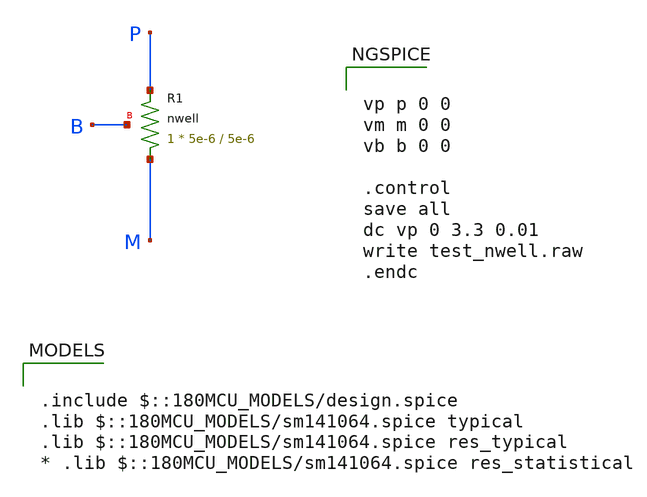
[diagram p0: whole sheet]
** sch_path: cells/xschem/tests/test_nwell.sch
* Copyright 2022 GlobalFoundries PDK Authors
* Licensed under the Apache License, Version 2.0 (the "License");
* you may not use this file except in compliance with the License.
* You may obtain a copy of the License at
* https://www.apache.org/licenses/LICENSE-2.0
* Unless required by applicable law or agreed to in writing, software
* distributed under the License is distributed on an "AS IS" BASIS,
* WITHOUT WARRANTIES OR CONDITIONS OF ANY KIND, either express or implied.
* See the License for the specific language governing permissions and
* limitations under the License.
**.subckt test_nwell
XR1 M P B nwell r_width=5e-6 r_length=5e-6 m=1
**** begin user architecture code

.include $::180MCU_MODELS/design.spice
.lib $::180MCU_MODELS/sm141064.spice typical
.lib $::180MCU_MODELS/sm141064.spice res_typical
* .lib $::180MCU_MODELS/sm141064.spice res_statistical



vp p 0 0
vm m 0 0
vb b 0 0

.control
save all
dc vp 0 3.3 0.01
write test_nwell.raw
.endc


**** end user architecture code
**.ends
.end
